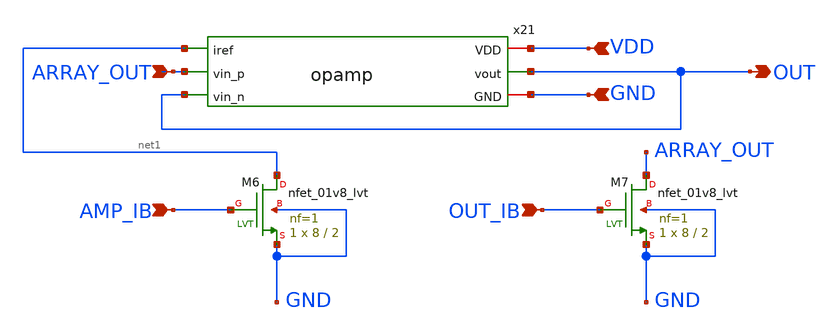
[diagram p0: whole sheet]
** sch_path: xschem/opamp_wrapper.sch
**.subckt opamp_wrapper ARRAY_OUT AMP_IB OUT_IB GND VDD OUT
*.ipin ARRAY_OUT
*.ipin AMP_IB
*.ipin OUT_IB
*.ipin GND
*.ipin VDD
*.opin OUT
x21 VDD net1 ARRAY_OUT OUT OUT GND opamp
XM6 net1 AMP_IB GND GND sky130_fd_pr__nfet_01v8_lvt L=2 W=8 nf=1 ad='int((nf+1)/2) * W/nf * 0.29' as='int((nf+2)/2) * W/nf * 0.29'
+ pd='2*int((nf+1)/2) * (W/nf + 0.29)' ps='2*int((nf+2)/2) * (W/nf + 0.29)' nrd='0.29 / W' nrs='0.29 / W'
+ sa=0 sb=0 sd=0 mult=1 m=1
XM7 ARRAY_OUT OUT_IB GND GND sky130_fd_pr__nfet_01v8_lvt L=2 W=8 nf=1 ad='int((nf+1)/2) * W/nf * 0.29'
+ as='int((nf+2)/2) * W/nf * 0.29' pd='2*int((nf+1)/2) * (W/nf + 0.29)' ps='2*int((nf+2)/2) * (W/nf + 0.29)'
+ nrd='0.29 / W' nrs='0.29 / W' sa=0 sb=0 sd=0 mult=1 m=1
**.ends

* expanding   symbol:  opamp.sym # of pins=6
** sym_path: xschem/opamp.sym
** sch_path: xschem/opamp.sch
.subckt opamp VDD iref vin_p vin_n vout GND
*.iopin VDD
*.iopin GND
*.ipin iref
*.opin vout
*.ipin vin_n
*.ipin vin_p
XM1 net1 vin_n net3 net3 sky130_fd_pr__pfet_01v8 L=0.3 W=3 nf=1 ad='W * 0.29' as='W * 0.29' pd='2 * (W + 0.29)'
+ ps='2 * (W + 0.29)' nrd='0.29 / W' nrs='0.29 / W' sa=0 sb=0 sd=0 mult=200 m=200
XM2 net2 vin_p net3 net3 sky130_fd_pr__pfet_01v8 L=0.3 W=3 nf=1 ad='W * 0.29' as='W * 0.29' pd='2 * (W + 0.29)'
+ ps='2 * (W + 0.29)' nrd='0.29 / W' nrs='0.29 / W' sa=0 sb=0 sd=0 mult=200 m=200
XM3 net1 net1 GND GND sky130_fd_pr__nfet_01v8 L=0.3 W=3 nf=1 ad='W * 0.29' as='W * 0.29' pd='2 * (W + 0.29)'
+ ps='2 * (W + 0.29)' nrd='0.29 / W' nrs='0.29 / W' sa=0 sb=0 sd=0 mult=30 m=30
XM4 net2 net1 GND GND sky130_fd_pr__nfet_01v8 L=0.3 W=3 nf=1 ad='W * 0.29' as='W * 0.29' pd='2 * (W + 0.29)'
+ ps='2 * (W + 0.29)' nrd='0.29 / W' nrs='0.29 / W' sa=0 sb=0 sd=0 mult=30 m=30
XM5 net3 iref VDD VDD sky130_fd_pr__pfet_01v8 L=0.3 W=3 nf=1 ad='W * 0.29' as='W * 0.29' pd='2 * (W + 0.29)'
+ ps='2 * (W + 0.29)' nrd='0.29 / W' nrs='0.29 / W' sa=0 sb=0 sd=0 mult=30 m=30
XM7 vout iref VDD VDD sky130_fd_pr__pfet_01v8 L=0.3 W=3 nf=1 ad='W * 0.29' as='W * 0.29' pd='2 * (W + 0.29)'
+ ps='2 * (W + 0.29)' nrd='0.29 / W' nrs='0.29 / W' sa=0 sb=0 sd=0 mult=150 m=150
XM8 iref iref VDD VDD sky130_fd_pr__pfet_01v8 L=0.3 W=3 nf=1 ad='W * 0.29' as='W * 0.29' pd='2 * (W + 0.29)'
+ ps='2 * (W + 0.29)' nrd='0.29 / W' nrs='0.29 / W' sa=0 sb=0 sd=0 mult=15 m=15
XM9 net4 VDD net2 GND sky130_fd_pr__nfet_01v8 L=0.15 W=0.75 nf=1 ad='W * 0.29' as='W * 0.29' pd='2 * (W + 0.29)'
+ ps='2 * (W + 0.29)' nrd='0.29 / W' nrs='0.29 / W' sa=0 sb=0 sd=0 mult=6 m=6
XC1 vout net4 sky130_fd_pr__cap_mim_m3_1 W=17.55 L=15 MF=6 m=6
XM6 vout net2 GND GND sky130_fd_pr__nfet_01v8 L=0.45 W=4.5 nf=1 ad='W * 0.29' as='W * 0.29' pd='2 * (W + 0.29)'
+ ps='2 * (W + 0.29)' nrd='0.29 / W' nrs='0.29 / W' sa=0 sb=0 sd=0 mult=150 m=150
.ends

.end
